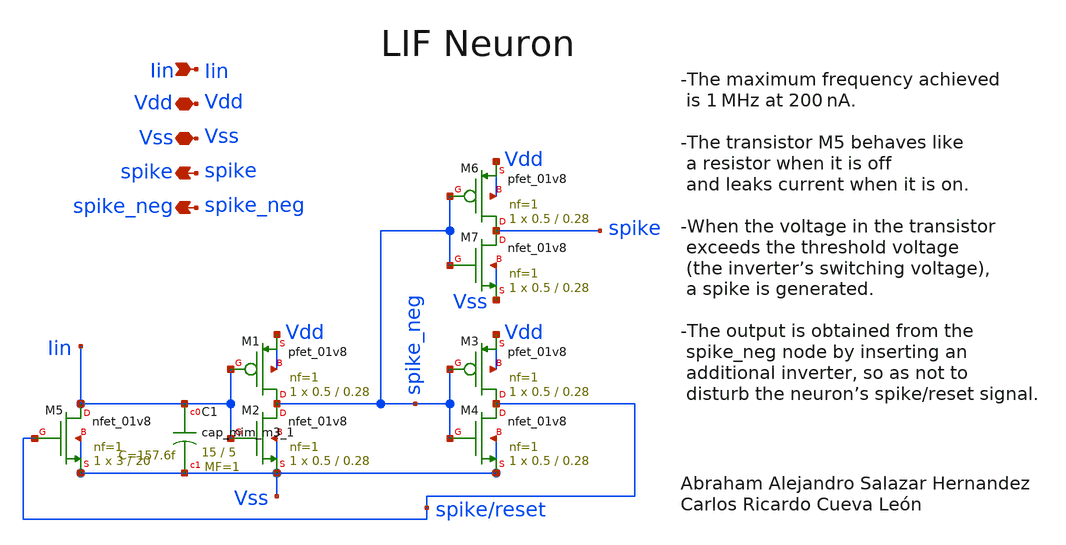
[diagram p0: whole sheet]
** sch_path: designs/libs/snn_analog/lif/sch/neurona.sch
**.subckt neurona Vdd Vss Iin spike spike_neg
*.iopin Vdd
*.iopin Vss
*.ipin Iin
*.opin spike
*.opin spike_neg
XM2 spike_neg Iin Vss Vss sky130_fd_pr__nfet_01v8 L=0.28 W=0.5 nf=1 ad='int((1 + 1)/2) * 0.5 / 1 * 0.29'
+ as='int((1 + 2)/2) * 0.5 / 1 * 0.29' pd='2*int((1 + 1)/2) * (0.5 / 1 + 0.29)' ps='2*int((1 + 2)/2) * (0.5 / 1 + 0.29)'
+ nrd='0.29 / 0.5 ' nrs='0.29 / 0.5 ' sa=0 sb=0 sd=0 mult=1 m=1
XM1 spike_neg Iin Vdd Vdd sky130_fd_pr__pfet_01v8 L=0.28 W=0.5 nf=1 ad='int((1 + 1)/2) * 0.5 / 1 * 0.29'
+ as='int((1 + 2)/2) * 0.5 / 1 * 0.29' pd='2*int((1 + 1)/2) * (0.5 / 1 + 0.29)' ps='2*int((1 + 2)/2) * (0.5 / 1 + 0.29)'
+ nrd='0.29 / 0.5 ' nrs='0.29 / 0.5 ' sa=0 sb=0 sd=0 mult=1 m=1
XM3 spike/reset spike_neg Vdd Vdd sky130_fd_pr__pfet_01v8 L=0.28 W=0.5 nf=1 ad='int((1 + 1)/2) * 0.5 / 1 * 0.29'
+ as='int((1 + 2)/2) * 0.5 / 1 * 0.29' pd='2*int((1 + 1)/2) * (0.5 / 1 + 0.29)' ps='2*int((1 + 2)/2) * (0.5 / 1 + 0.29)'
+ nrd='0.29 / 0.5 ' nrs='0.29 / 0.5 ' sa=0 sb=0 sd=0 mult=1 m=1
XM4 spike/reset spike_neg Vss Vss sky130_fd_pr__nfet_01v8 L=0.28 W=0.5 nf=1 ad='int((1 + 1)/2) * 0.5 / 1 * 0.29'
+ as='int((1 + 2)/2) * 0.5 / 1 * 0.29' pd='2*int((1 + 1)/2) * (0.5 / 1 + 0.29)' ps='2*int((1 + 2)/2) * (0.5 / 1 + 0.29)'
+ nrd='0.29 / 0.5 ' nrs='0.29 / 0.5 ' sa=0 sb=0 sd=0 mult=1 m=1
XM5 Iin spike/reset Vss Vss sky130_fd_pr__nfet_01v8 L=20 W=3 nf=1 ad='int((1 + 1)/2) * 3 / 1 * 0.29'
+ as='int((1 + 2)/2) * 3 / 1 * 0.29' pd='2*int((1 + 1)/2) * (3 / 1 + 0.29)' ps='2*int((1 + 2)/2) * (3 / 1 + 0.29)'
+ nrd='0.29 / 3 ' nrs='0.29 / 3 ' sa=0 sb=0 sd=0 mult=1 m=1
XM6 spike spike_neg Vdd Vdd sky130_fd_pr__pfet_01v8 L=0.28 W=0.5 nf=1 ad='int((1 + 1)/2) * 0.5 / 1 * 0.29'
+ as='int((1 + 2)/2) * 0.5 / 1 * 0.29' pd='2*int((1 + 1)/2) * (0.5 / 1 + 0.29)' ps='2*int((1 + 2)/2) * (0.5 / 1 + 0.29)'
+ nrd='0.29 / 0.5 ' nrs='0.29 / 0.5 ' sa=0 sb=0 sd=0 mult=1 m=1
XM7 spike spike_neg Vss Vss sky130_fd_pr__nfet_01v8 L=0.28 W=0.5 nf=1 ad='int((1 + 1)/2) * 0.5 / 1 * 0.29'
+ as='int((1 + 2)/2) * 0.5 / 1 * 0.29' pd='2*int((1 + 1)/2) * (0.5 / 1 + 0.29)' ps='2*int((1 + 2)/2) * (0.5 / 1 + 0.29)'
+ nrd='0.29 / 0.5 ' nrs='0.29 / 0.5 ' sa=0 sb=0 sd=0 mult=1 m=1
XC1 Iin Vss sky130_fd_pr__cap_mim_m3_1 W=15 L=5 MF=1 m=1
**.ends
.end
